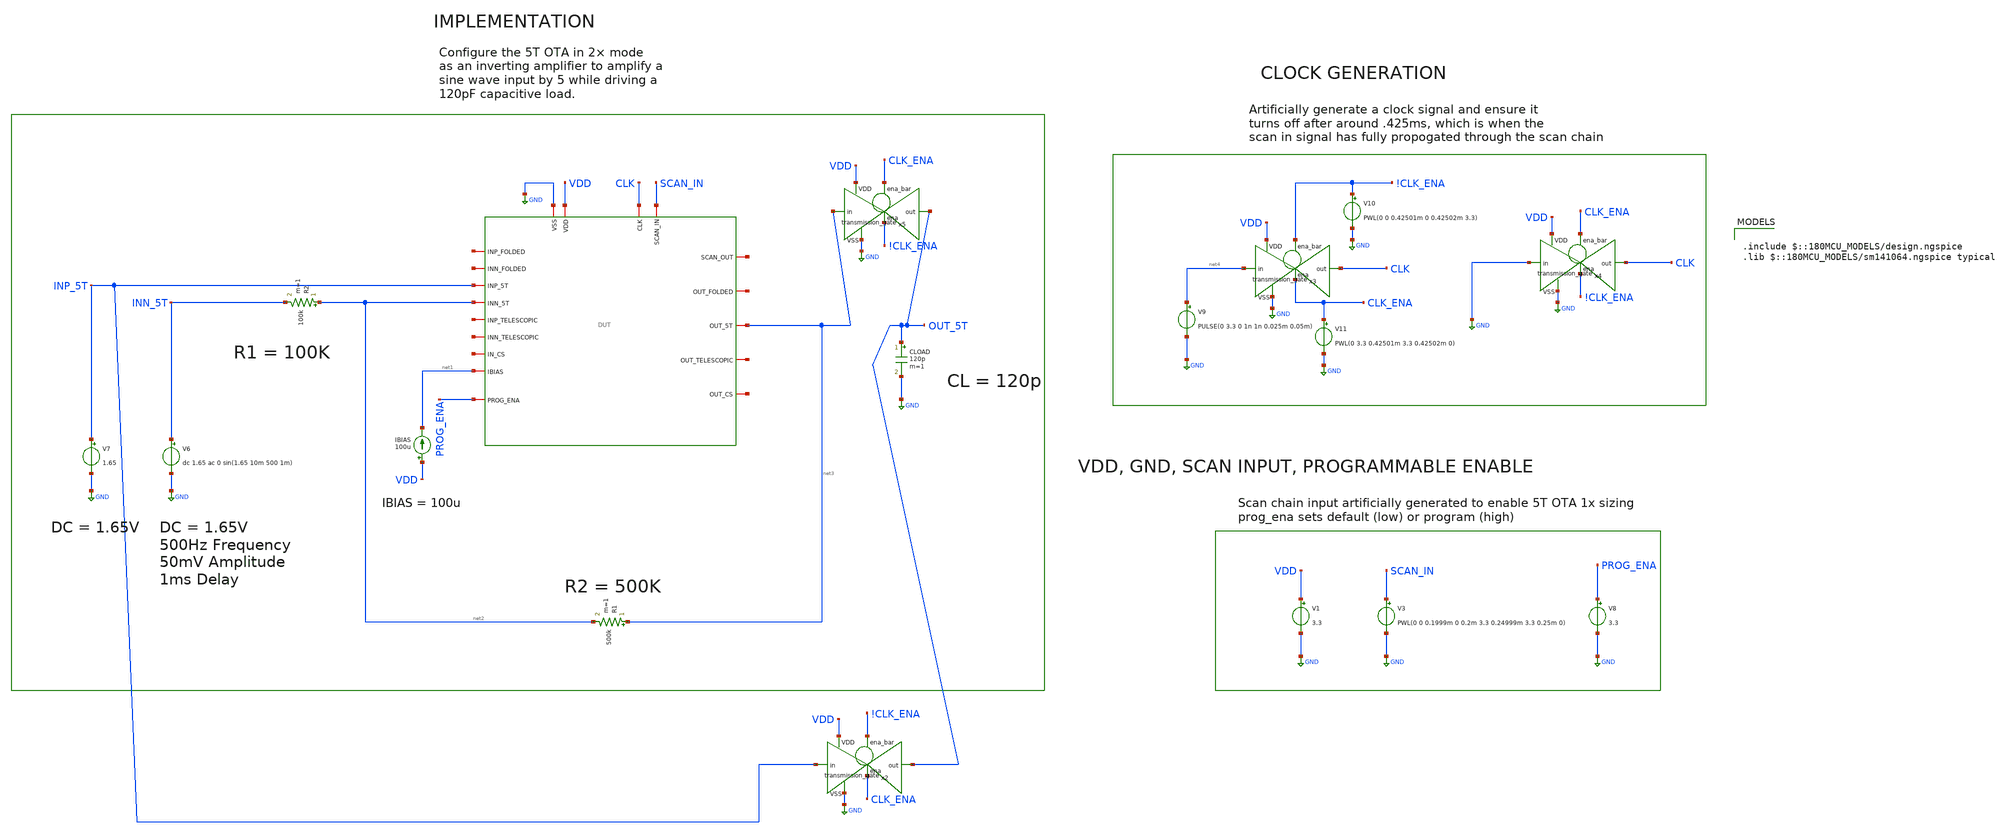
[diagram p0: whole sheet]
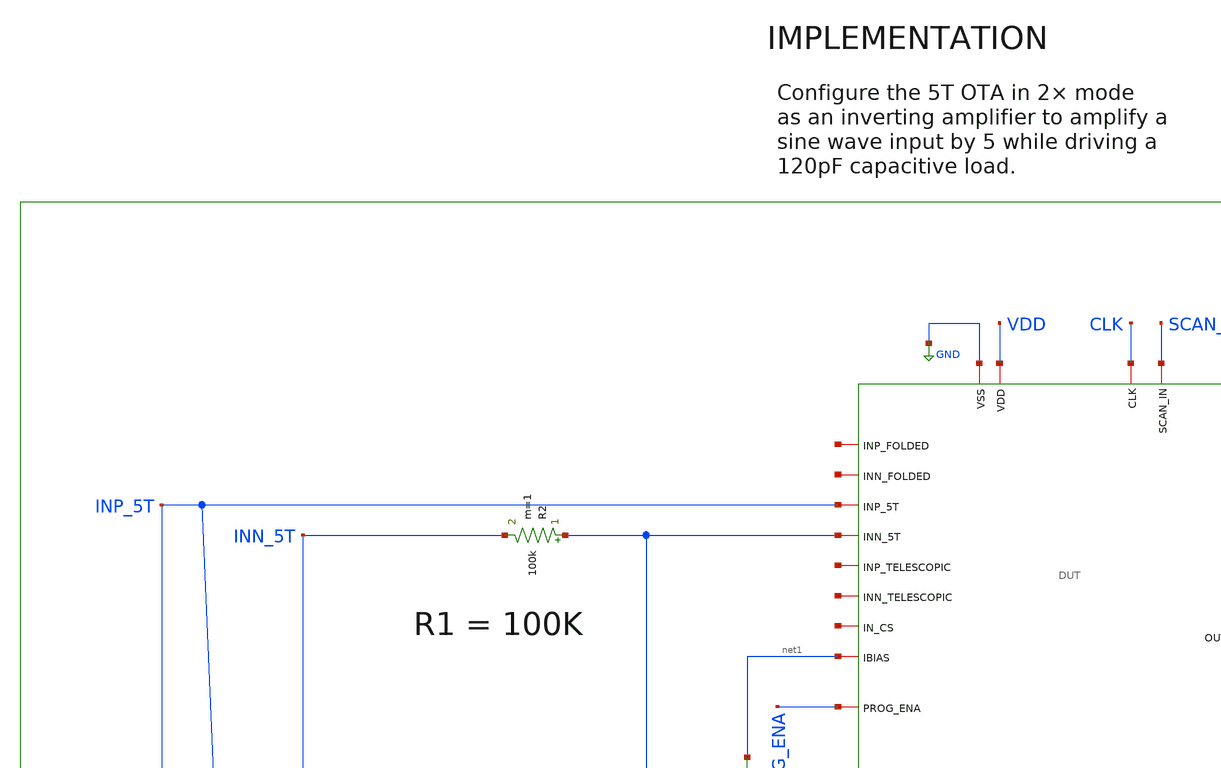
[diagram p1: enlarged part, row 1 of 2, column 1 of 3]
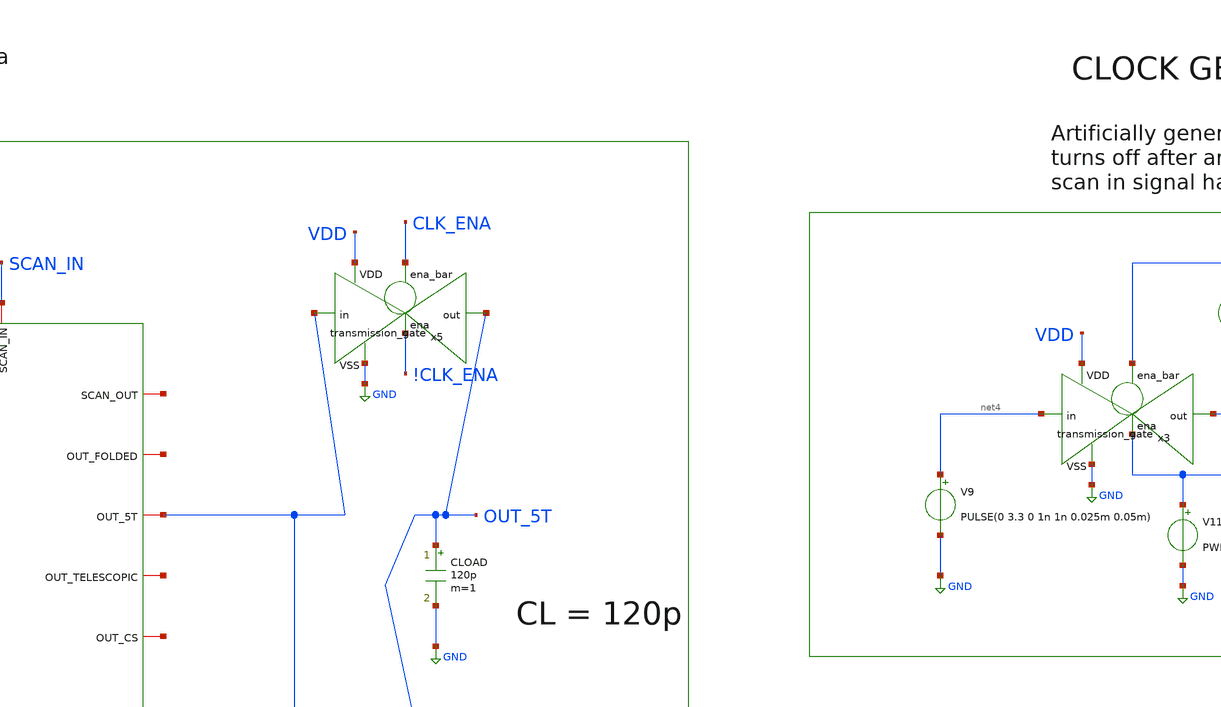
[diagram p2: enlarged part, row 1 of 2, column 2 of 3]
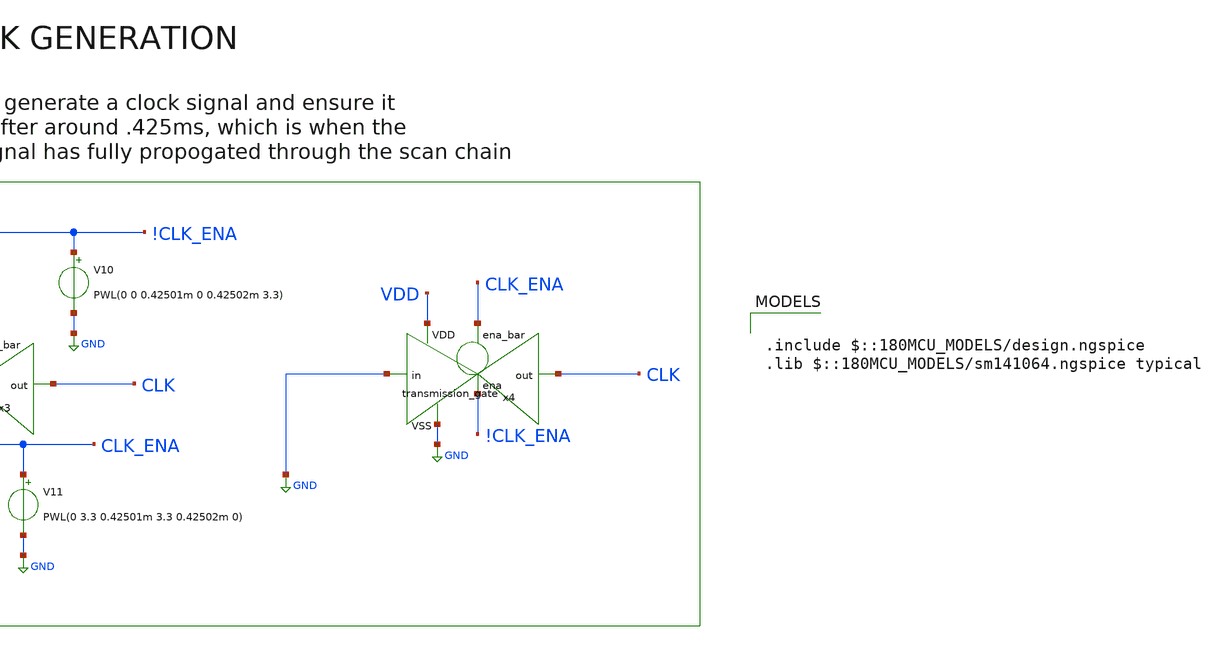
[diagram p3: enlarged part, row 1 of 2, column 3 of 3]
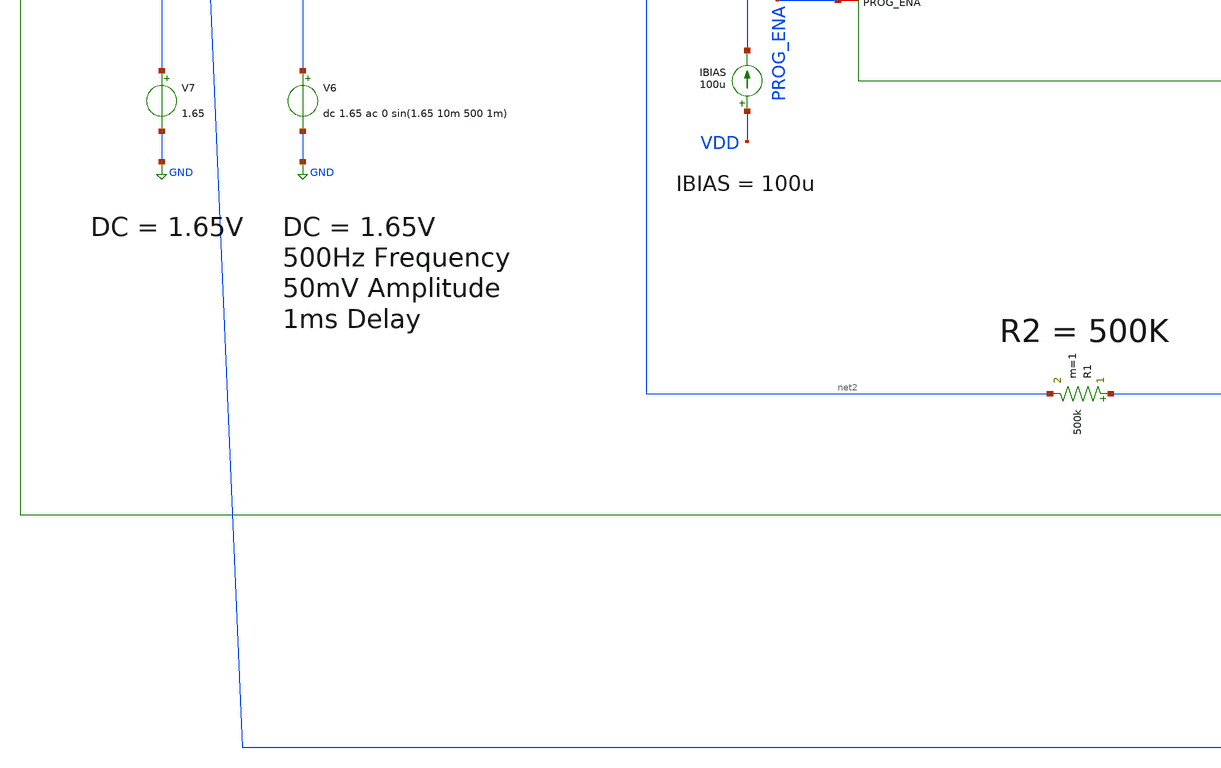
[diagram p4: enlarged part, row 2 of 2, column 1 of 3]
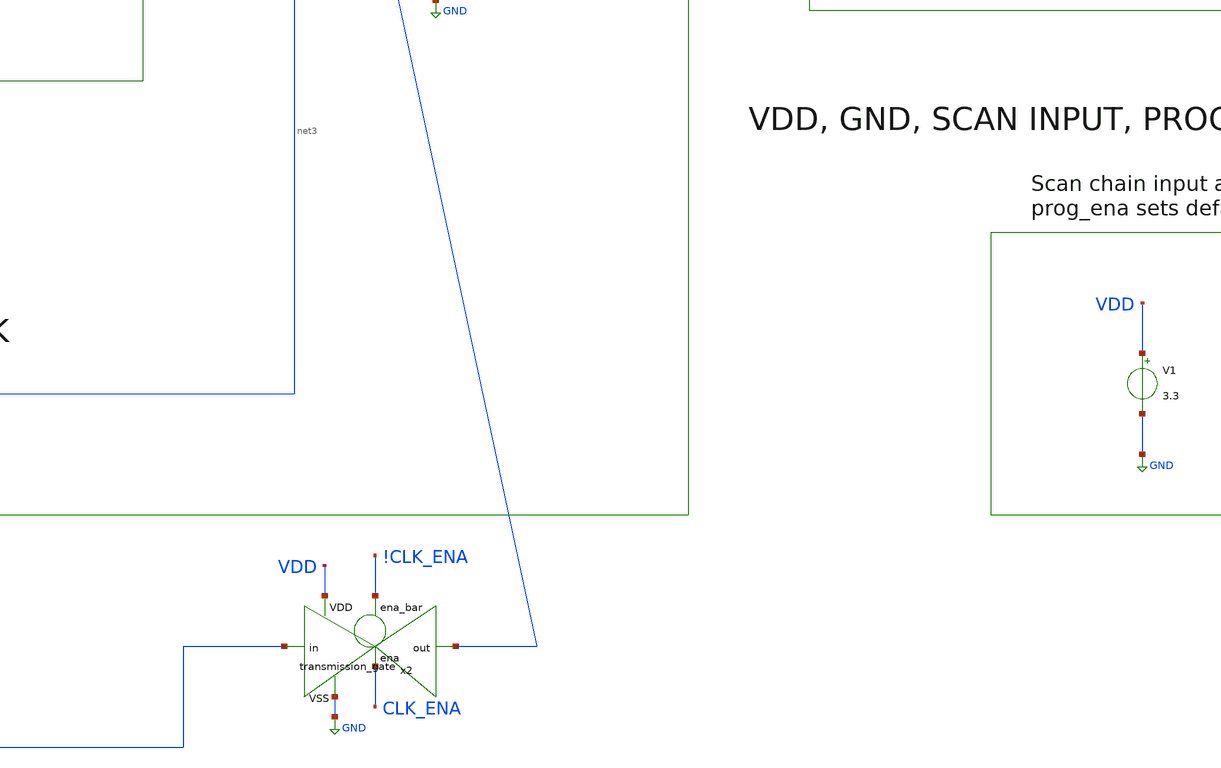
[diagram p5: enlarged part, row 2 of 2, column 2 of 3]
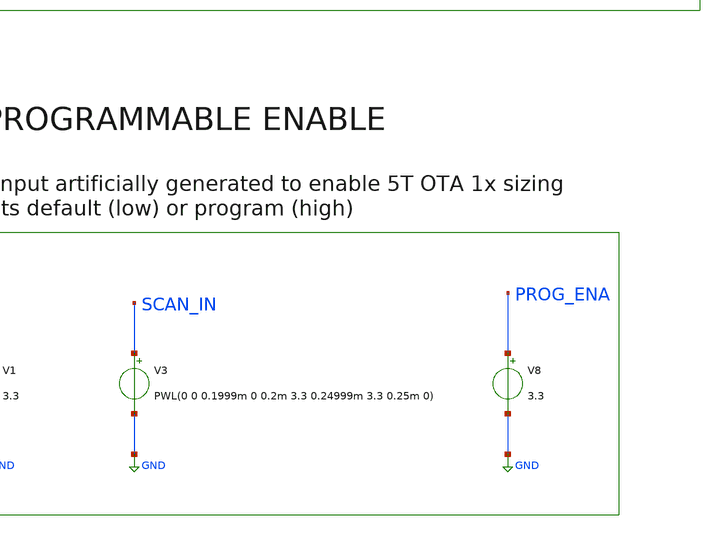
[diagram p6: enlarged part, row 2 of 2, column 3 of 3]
** sch_path: designs/libs/verification/ota_5t/2x_sizing/5t_2x_inverting_amplifier_tb_startupClean.sch
**.subckt 5t_2x_inverting_amplifier_tb_startupClean
V3 SCAN_IN GND PWL(0 0 0.1999m 0 0.2m 3.3 0.24999m 3.3 0.25m 0)
V1 VDD GND 3.3
IBIAS VDD net1 100u
V7 INP_5T GND 1.65
CLOAD OUT_5T GND 120p m=1
R2 net2 INN_5T 100k m=1
V6 INN_5T GND dc 1.65 ac 0 sin(1.65 10m 500 1m)
R1 net3 net2 500k m=1
x1 CLK net5 SCAN_IN GND VDD net6 net7 net3 net1 net8 INP_5T net2 net9 net10 net11 net12 net13
+ PROG_ENA DUT
V8 PROG_ENA GND 3.3
V9 net4 GND PULSE(0 3.3 0 1n 1n 0.025m 0.05m)
x3 !CLK_ENA VDD CLK net4 GND CLK_ENA transmission_gate
V10 !CLK_ENA GND PWL(0 0 0.42501m 0 0.42502m 3.3)
V11 CLK_ENA GND PWL(0 3.3 0.42501m 3.3 0.42502m 0)
x4 CLK_ENA VDD CLK GND GND !CLK_ENA transmission_gate
x2 !CLK_ENA VDD OUT_5T INP_5T GND CLK_ENA transmission_gate
x5 CLK_ENA VDD OUT_5T net3 GND !CLK_ENA transmission_gate
**** begin user architecture code

.include $::180MCU_MODELS/design.ngspice
.lib $::180MCU_MODELS/sm141064.ngspice typical



.control
tran 1u 5m

set color0 = white
set color1 = black
plot v(out_5T) v(inn_5T)
plot v(CLK)
plot v(CLK_ENA)

meas tran vout_pp pp v(out_5T) from=2m to=5m
meas tran vin_pp pp v(inn_5T) from=2m to=5m
let gain = vout_pp / vin_pp
print gain

meas tran vout_dc avg v(out_5T) from=2m to=5m
meas tran vin_dc avg v(inn_5T) from=2m to=5m
let dc_offset = vout_dc - vin_dc
let input_offset = dc_offset / 6
print vout_dc vin_dc dc_offset input_offset

let ideal_gain = 5
let gain_error_pct = (ideal_gain - gain) / ideal_gain * 100
print gain_error_pct

meas tran idd avg i(v1) from=2m to=5m
let power = abs(idd) * 3.3
print idd power
.endc


**** end user architecture code
**.ends
.GLOBAL GND
.end
